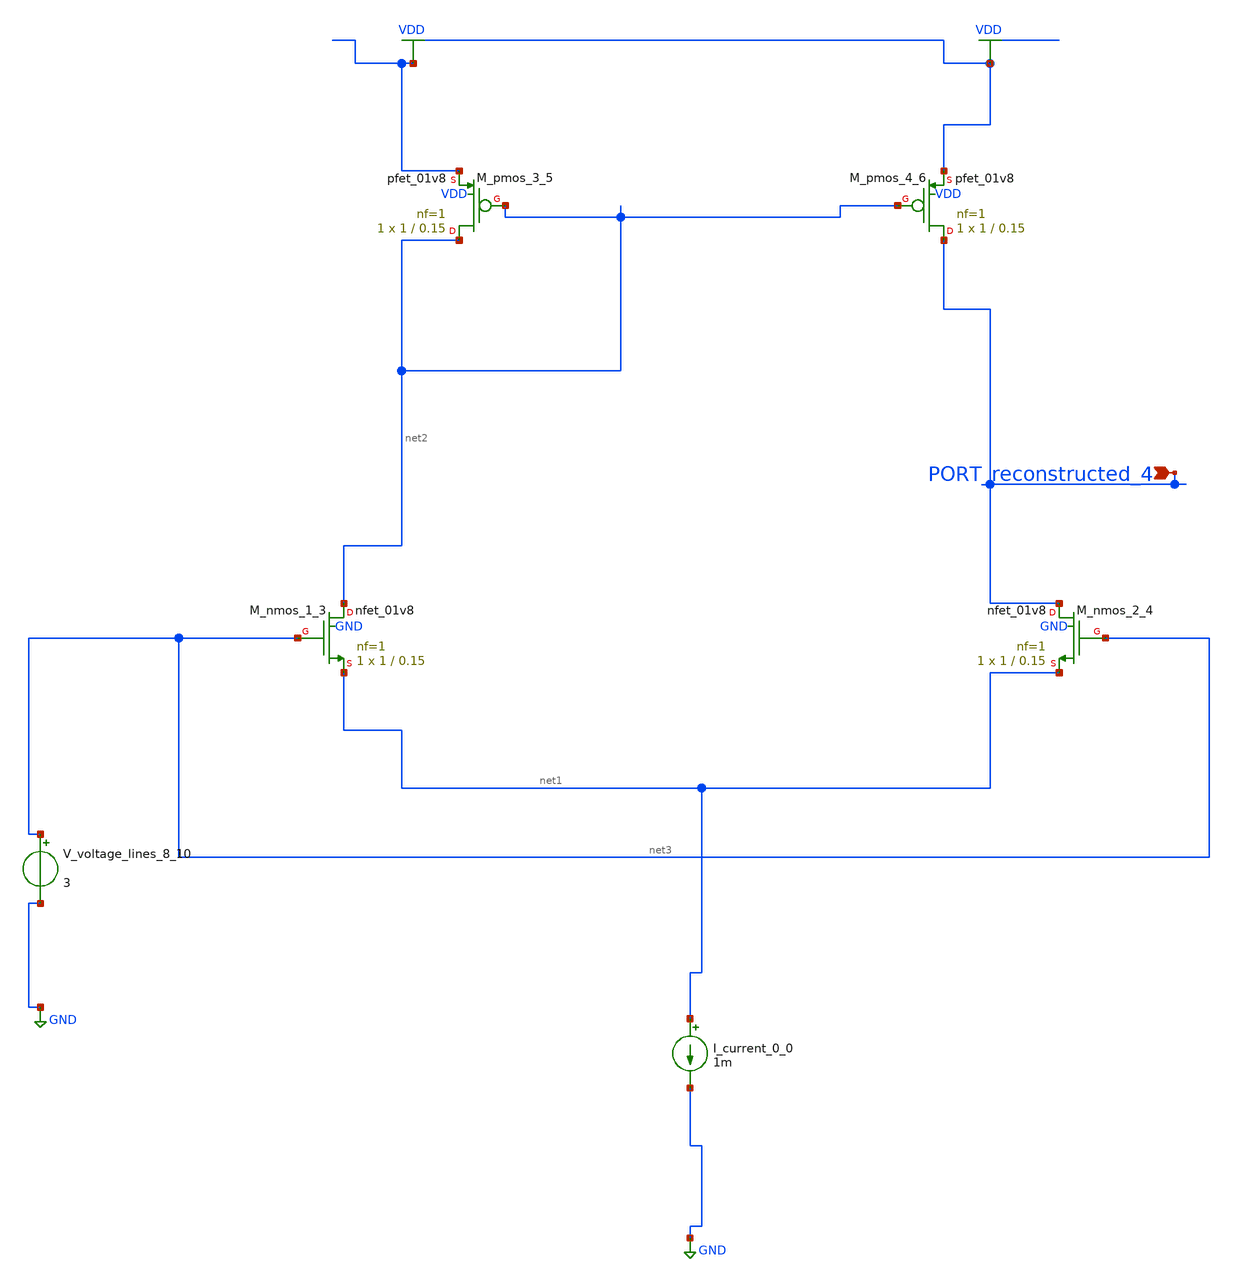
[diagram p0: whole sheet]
** sch_path: schematics/AMSNet/295.sch
**.subckt 295 PORT_reconstructed_4
*.ipin PORT_reconstructed_4
I_current_0_0 net1 GND 1m
XM_nmos_1_3 net2 net3 net1 GND sky130_fd_pr__nfet_01v8 L=0.15 W=1 nf=1 ad='int((1 + 1)/2) * 1 / 1 * 0.29'
+ as='int((1 + 2)/2) * 1 / 1 * 0.29' pd='2*int((1 + 1)/2) * (1 / 1 + 0.29)' ps='2*int((1 + 2)/2) * (1 / 1 + 0.29)'
+ nrd='0.29 / 1 ' nrs='0.29 / 1 ' sa=0 sb=0 sd=0 mult=1 m=1
XM_nmos_2_4 PORT_reconstructed_4 net3 net1 GND sky130_fd_pr__nfet_01v8 L=0.15 W=1 nf=1 ad='int((1 + 1)/2) * 1 / 1 * 0.29'
+ as='int((1 + 2)/2) * 1 / 1 * 0.29' pd='2*int((1 + 1)/2) * (1 / 1 + 0.29)' ps='2*int((1 + 2)/2) * (1 / 1 + 0.29)'
+ nrd='0.29 / 1 ' nrs='0.29 / 1 ' sa=0 sb=0 sd=0 mult=1 m=1
XM_pmos_3_5 net2 net2 VDD VDD sky130_fd_pr__pfet_01v8 L=0.15 W=1 nf=1 ad='int((1 + 1)/2) * 1 / 1 * 0.29'
+ as='int((1 + 2)/2) * 1 / 1 * 0.29' pd='2*int((1 + 1)/2) * (1 / 1 + 0.29)' ps='2*int((1 + 2)/2) * (1 / 1 + 0.29)'
+ nrd='0.29 / 1 ' nrs='0.29 / 1 ' sa=0 sb=0 sd=0 mult=1 m=1
XM_pmos_4_6 PORT_reconstructed_4 net2 VDD VDD sky130_fd_pr__pfet_01v8 L=0.15 W=1 nf=1 ad='int((1 + 1)/2) * 1 / 1 * 0.29'
+ as='int((1 + 2)/2) * 1 / 1 * 0.29' pd='2*int((1 + 1)/2) * (1 / 1 + 0.29)' ps='2*int((1 + 2)/2) * (1 / 1 + 0.29)'
+ nrd='0.29 / 1 ' nrs='0.29 / 1 ' sa=0 sb=0 sd=0 mult=1 m=1
V_voltage_lines_8_10 net3 GND 3
**.ends
.GLOBAL GND
.GLOBAL VDD
.end
